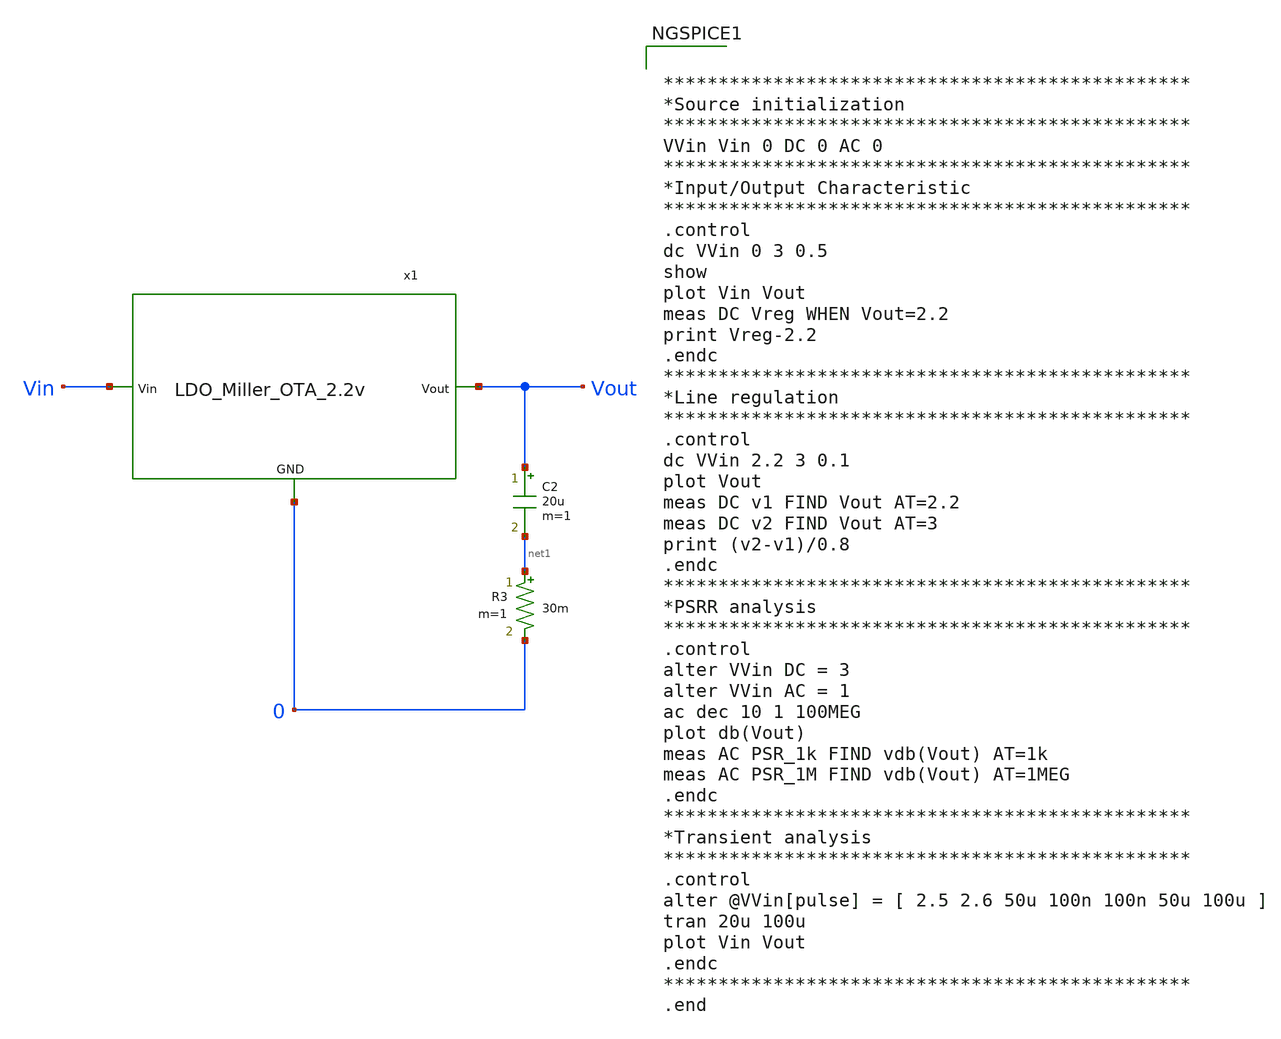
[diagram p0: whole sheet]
** sch_path: Analog_blocks/Analog_Blocks/LDO/Testbench/LDO_Miller_2.2v_meas.sch
**.subckt LDO_Miller_2.2v_meas
C2 Vout net1 20u m=1
R3 net1 0 30m m=1
x1 Vin Vout 0 LDO_Miller_OTA_2.2v
**** begin user architecture code


************************************************
*Source initialization
************************************************
VVin Vin 0 DC 0 AC 0
************************************************
*Input/Output Characteristic
************************************************
.control
dc VVin 0 3 0.5
show
plot Vin Vout
meas DC Vreg WHEN Vout=2.2
print Vreg-2.2
.endc
************************************************
*Line regulation
************************************************
.control
dc VVin 2.2 3 0.1
plot Vout
meas DC v1 FIND Vout AT=2.2
meas DC v2 FIND Vout AT=3
print (v2-v1)/0.8
.endc
************************************************
*PSRR analysis
************************************************
.control
alter VVin DC = 3
alter VVin AC = 1
ac dec 10 1 100MEG
plot db(Vout)
meas AC PSR_1k FIND vdb(Vout) AT=1k
meas AC PSR_1M FIND vdb(Vout) AT=1MEG
.endc
************************************************
*Transient analysis
************************************************
.control
alter @VVin[pulse] = [ 2.5 2.6 50u 100n 100n 50u 100u ]
tran 20u 100u
plot Vin Vout
.endc
************************************************
.end



.include ~/Analog_blocks/models/skywater-pdk/libraries/sky130_fd_pr/latest/cells/nfet_01v8/sky130_fd_pr__nfet_01v8__tt.corner.spice
.include ~/Analog_blocks/models/skywater-pdk/libraries/sky130_fd_pr/latest/cells/nfet_01v8_lvt/sky130_fd_pr__nfet_01v8_lvt__tt.corner.spice
.include ~/Analog_blocks/models/skywater-pdk/libraries/sky130_fd_pr/latest/cells/pfet_01v8/sky130_fd_pr__pfet_01v8__tt.corner.spice
.include ~/Analog_blocks/models/skywater-pdk/libraries/sky130_fd_pr/latest/cells/nfet_03v3_nvt/sky130_fd_pr__nfet_03v3_nvt__tt.corner.spice
.include ~/Analog_blocks/models/skywater-pdk/libraries/sky130_fd_pr/latest/cells/nfet_05v0_nvt/sky130_fd_pr__nfet_05v0_nvt__tt.corner.spice
.include ~/Analog_blocks/models/skywater-pdk/libraries/sky130_fd_pr/latest/cells/esd_nfet_01v8/sky130_fd_pr__esd_nfet_01v8__tt.corner.spice
.include ~/Analog_blocks/models/skywater-pdk/libraries/sky130_fd_pr/latest/cells/pfet_01v8_lvt/sky130_fd_pr__pfet_01v8_lvt__tt.corner.spice
.include ~/Analog_blocks/models/skywater-pdk/libraries/sky130_fd_pr/latest/cells/pfet_01v8_hvt/sky130_fd_pr__pfet_01v8_hvt__tt.corner.spice
.include ~/Analog_blocks/models/skywater-pdk/libraries/sky130_fd_pr/latest/cells/esd_pfet_g5v0d10v5/sky130_fd_pr__esd_pfet_g5v0d10v5__tt.corner.spice
.include ~/Analog_blocks/models/skywater-pdk/libraries/sky130_fd_pr/latest/cells/pfet_g5v0d10v5/sky130_fd_pr__pfet_g5v0d10v5__tt.corner.spice
.include ~/Analog_blocks/models/skywater-pdk/libraries/sky130_fd_pr/latest/cells/pfet_g5v0d16v0/sky130_fd_pr__pfet_g5v0d16v0__tt.corner.spice
.include ~/Analog_blocks/models/skywater-pdk/libraries/sky130_fd_pr/latest/cells/nfet_g5v0d10v5/sky130_fd_pr__nfet_g5v0d10v5__tt.corner.spice
.include ~/Analog_blocks/models/skywater-pdk/libraries/sky130_fd_pr/latest/cells/nfet_g5v0d16v0/sky130_fd_pr__nfet_g5v0d16v0__tt_discrete.corner.spice
.include ~/Analog_blocks/models/skywater-pdk/libraries/sky130_fd_pr/latest/cells/esd_nfet_g5v0d10v5/sky130_fd_pr__esd_nfet_g5v0d10v5__tt.corner.spice
.include ~/Analog_blocks/models/skywater-pdk/libraries/sky130_fd_pr/latest/models/corners/tt/nonfet.spice
* Mismatch parameters
.include ~/Analog_blocks/models/skywater-pdk/libraries/sky130_fd_pr/latest/cells/nfet_01v8/sky130_fd_pr__nfet_01v8__mismatch.corner.spice
.include ~/Analog_blocks/models/skywater-pdk/libraries/sky130_fd_pr/latest/cells/pfet_01v8/sky130_fd_pr__pfet_01v8__mismatch.corner.spice
.include ~/Analog_blocks/models/skywater-pdk/libraries/sky130_fd_pr/latest/cells/nfet_01v8_lvt/sky130_fd_pr__nfet_01v8_lvt__mismatch.corner.spice
.include ~/Analog_blocks/models/skywater-pdk/libraries/sky130_fd_pr/latest/cells/pfet_01v8_lvt/sky130_fd_pr__pfet_01v8_lvt__mismatch.corner.spice
.include ~/Analog_blocks/models/skywater-pdk/libraries/sky130_fd_pr/latest/cells/pfet_01v8_hvt/sky130_fd_pr__pfet_01v8_hvt__mismatch.corner.spice
.include ~/Analog_blocks/models/skywater-pdk/libraries/sky130_fd_pr/latest/cells/nfet_g5v0d10v5/sky130_fd_pr__nfet_g5v0d10v5__mismatch.corner.spice
.include ~/Analog_blocks/models/skywater-pdk/libraries/sky130_fd_pr/latest/cells/pfet_g5v0d10v5/sky130_fd_pr__pfet_g5v0d10v5__mismatch.corner.spice
.include ~/Analog_blocks/models/skywater-pdk/libraries/sky130_fd_pr/latest/cells/nfet_05v0_nvt/sky130_fd_pr__nfet_05v0_nvt__mismatch.corner.spice
.include ~/Analog_blocks/models/skywater-pdk/libraries/sky130_fd_pr/latest/cells/nfet_03v3_nvt/sky130_fd_pr__nfet_03v3_nvt__mismatch.corner.spice
* Resistor
.include ~/Analog_blocks/models/skywater-pdk/libraries/sky130_fd_pr/latest/models/r+c/res_typical__cap_typical.spice
.include ~/Analog_blocks/models/skywater-pdk/libraries/sky130_fd_pr/latest/models/r+c/res_typical__cap_typical__lin.spice
* Special cells
.include ~/Analog_blocks/models/skywater-pdk/libraries/sky130_fd_pr/latest/models/corners/tt/specialized_cells.spice
* All models
.include ~/Analog_blocks/models/skywater-pdk/libraries/sky130_fd_pr/latest/models/all.spice
* Corner
.include ~/Analog_blocks/models/skywater-pdk/libraries/sky130_fd_pr/latest/models/corners/tt/rf.spice

**** end user architecture code
**.ends
.end
